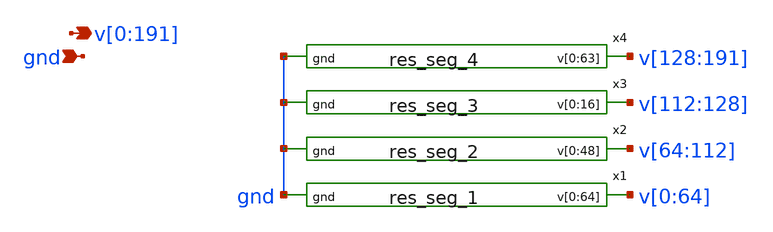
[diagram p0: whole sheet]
** sch_path: xschem/rstring.sch
**.subckt rstring
*+ v[0],v[1],v[2],v[3],v[4],v[5],v[6],v[7],v[8],v[9],v[10],v[11],v[12],v[13],v[14],v[15],v[16],v[17],v[18],v[19],v[20],v[21],v[22],v[23],v[24],v[25],v[26],v[27],v[28],v[29],v[30],v[31],v[32],v[33],v[34],v[35],v[36],v[37],v[38],v[39],v[40],v[41],v[42],v[43],v[44],v[45],v[46],v[47],v[48],v[49],v[50],v[51],v[52],v[53],v[54],v[55],v[56],v[57],v[58],v[59],v[60],v[61],v[62],v[63],v[64],v[65],v[66],v[67],v[68],v[69],v[70],v[71],v[72],v[73],v[74],v[75],v[76],v[77],v[78],v[79],v[80],v[81],v[82],v[83],v[84],v[85],v[86],v[87],v[88],v[89],v[90],v[91],v[92],v[93],v[94],v[95],v[96],v[97],v[98],v[99],v[100],v[101],v[102],v[103],v[104],v[105],v[106],v[107],v[108],v[109],v[110],v[111],v[112],v[113],v[114],v[115],v[116],v[117],v[118],v[119],v[120],v[121],v[122],v[123],v[124],v[125],v[126],v[127],v[128],v[129],v[130],v[131],v[132],v[133],v[134],v[135],v[136],v[137],v[138],v[139],v[140],v[141],v[142],v[143],v[144],v[145],v[146],v[147],v[148],v[149],v[150],v[151],v[152],v[153],v[154],v[155],v[156],v[157],v[158],v[159],v[160],v[161],v[162],v[163],v[164],v[165],v[166],v[167],v[168],v[169],v[170],v[171],v[172],v[173],v[174],v[175],v[176],v[177],v[178],v[179],v[180],v[181],v[182],v[183],v[184],v[185],v[186],v[187],v[188],v[189],v[190],v[191] gnd
*.opin
*+ v[0],v[1],v[2],v[3],v[4],v[5],v[6],v[7],v[8],v[9],v[10],v[11],v[12],v[13],v[14],v[15],v[16],v[17],v[18],v[19],v[20],v[21],v[22],v[23],v[24],v[25],v[26],v[27],v[28],v[29],v[30],v[31],v[32],v[33],v[34],v[35],v[36],v[37],v[38],v[39],v[40],v[41],v[42],v[43],v[44],v[45],v[46],v[47],v[48],v[49],v[50],v[51],v[52],v[53],v[54],v[55],v[56],v[57],v[58],v[59],v[60],v[61],v[62],v[63],v[64],v[65],v[66],v[67],v[68],v[69],v[70],v[71],v[72],v[73],v[74],v[75],v[76],v[77],v[78],v[79],v[80],v[81],v[82],v[83],v[84],v[85],v[86],v[87],v[88],v[89],v[90],v[91],v[92],v[93],v[94],v[95],v[96],v[97],v[98],v[99],v[100],v[101],v[102],v[103],v[104],v[105],v[106],v[107],v[108],v[109],v[110],v[111],v[112],v[113],v[114],v[115],v[116],v[117],v[118],v[119],v[120],v[121],v[122],v[123],v[124],v[125],v[126],v[127],v[128],v[129],v[130],v[131],v[132],v[133],v[134],v[135],v[136],v[137],v[138],v[139],v[140],v[141],v[142],v[143],v[144],v[145],v[146],v[147],v[148],v[149],v[150],v[151],v[152],v[153],v[154],v[155],v[156],v[157],v[158],v[159],v[160],v[161],v[162],v[163],v[164],v[165],v[166],v[167],v[168],v[169],v[170],v[171],v[172],v[173],v[174],v[175],v[176],v[177],v[178],v[179],v[180],v[181],v[182],v[183],v[184],v[185],v[186],v[187],v[188],v[189],v[190],v[191]
*.ipin gnd
x1 v[0] v[1] v[2] v[3] v[4] v[5] v[6] v[7] v[8] v[9] v[10] v[11] v[12] v[13] v[14] v[15] v[16] v[17]
+ v[18] v[19] v[20] v[21] v[22] v[23] v[24] v[25] v[26] v[27] v[28] v[29] v[30] v[31] v[32] v[33] v[34]
+ v[35] v[36] v[37] v[38] v[39] v[40] v[41] v[42] v[43] v[44] v[45] v[46] v[47] v[48] v[49] v[50] v[51]
+ v[52] v[53] v[54] v[55] v[56] v[57] v[58] v[59] v[60] v[61] v[62] v[63] v[64] gnd res_seg_1
x2 v[64] v[65] v[66] v[67] v[68] v[69] v[70] v[71] v[72] v[73] v[74] v[75] v[76] v[77] v[78] v[79]
+ v[80] v[81] v[82] v[83] v[84] v[85] v[86] v[87] v[88] v[89] v[90] v[91] v[92] v[93] v[94] v[95] v[96]
+ v[97] v[98] v[99] v[100] v[101] v[102] v[103] v[104] v[105] v[106] v[107] v[108] v[109] v[110] v[111]
+ v[112] gnd res_seg_2
x3 v[112] v[113] v[114] v[115] v[116] v[117] v[118] v[119] v[120] v[121] v[122] v[123] v[124] v[125]
+ v[126] v[127] v[128] gnd res_seg_3
x4 v[128] v[129] v[130] v[131] v[132] v[133] v[134] v[135] v[136] v[137] v[138] v[139] v[140] v[141]
+ v[142] v[143] v[144] v[145] v[146] v[147] v[148] v[149] v[150] v[151] v[152] v[153] v[154] v[155] v[156]
+ v[157] v[158] v[159] v[160] v[161] v[162] v[163] v[164] v[165] v[166] v[167] v[168] v[169] v[170] v[171]
+ v[172] v[173] v[174] v[175] v[176] v[177] v[178] v[179] v[180] v[181] v[182] v[183] v[184] v[185] v[186]
+ v[187] v[188] v[189] v[190] v[191] gnd res_seg_4
**.ends

* expanding   symbol:  res_seg_1.sym # of pins=2
** sym_path: xschem/res_seg_1.sym
** sch_path: xschem/res_seg_1.sch
.subckt res_seg_1 v[0] v[1] v[2] v[3] v[4] v[5] v[6] v[7] v[8] v[9] v[10] v[11] v[12] v[13] v[14]
+ v[15] v[16] v[17] v[18] v[19] v[20] v[21] v[22] v[23] v[24] v[25] v[26] v[27] v[28] v[29] v[30] v[31]
+ v[32] v[33] v[34] v[35] v[36] v[37] v[38] v[39] v[40] v[41] v[42] v[43] v[44] v[45] v[46] v[47] v[48]
+ v[49] v[50] v[51] v[52] v[53] v[54] v[55] v[56] v[57] v[58] v[59] v[60] v[61] v[62] v[63] v[64] gnd
*.opin
*+ v[0],v[1],v[2],v[3],v[4],v[5],v[6],v[7],v[8],v[9],v[10],v[11],v[12],v[13],v[14],v[15],v[16],v[17],v[18],v[19],v[20],v[21],v[22],v[23],v[24],v[25],v[26],v[27],v[28],v[29],v[30],v[31],v[32],v[33],v[34],v[35],v[36],v[37],v[38],v[39],v[40],v[41],v[42],v[43],v[44],v[45],v[46],v[47],v[48],v[49],v[50],v[51],v[52],v[53],v[54],v[55],v[56],v[57],v[58],v[59],v[60],v[61],v[62],v[63],v[64]
*.ipin gnd
XR1 v[1] v[0] gnd sky130_fd_pr__res_xhigh_po_0p35 L=0.8375 mult=1 m=1
XR2 v[2] v[1] gnd sky130_fd_pr__res_xhigh_po_0p35 L=0.7349 mult=1 m=1
XR3 v[3] v[2] gnd sky130_fd_pr__res_xhigh_po_0p35 L=0.6495 mult=1 m=1
XR4 v[4] v[3] gnd sky130_fd_pr__res_xhigh_po_0p35 L=0.5897 mult=1 m=1
XR8 v[7] v[8] gnd sky130_fd_pr__res_xhigh_po_0p69 L=0.8761 mult=1 m=1
XR9 v[8] v[9] gnd sky130_fd_pr__res_xhigh_po_0p69 L=0.8255 mult=1 m=1
XR10 v[9] v[10] gnd sky130_fd_pr__res_xhigh_po_0p69 L=0.775 mult=1 m=1
XR11 v[10] v[11] gnd sky130_fd_pr__res_xhigh_po_0p69 L=0.7413 mult=1 m=1
XR12 v[11] v[12] gnd sky130_fd_pr__res_xhigh_po_0p69 L=0.7076 mult=1 m=1
XR13 v[12] v[13] gnd sky130_fd_pr__res_xhigh_po_0p69 L=0.6739 mult=1 m=1
XR14 v[13] v[14] gnd sky130_fd_pr__res_xhigh_po_0p69 L=0.657 mult=1 m=1
XR15 v[14] v[15] gnd sky130_fd_pr__res_xhigh_po_0p69 L=0.6234 mult=1 m=1
XR16 v[15] v[16] gnd sky130_fd_pr__res_xhigh_po_0p69 L=0.6065 mult=1 m=1
XR17 v[16] v[17] gnd sky130_fd_pr__res_xhigh_po_0p69 L=0.5728 mult=1 m=1
XR19 v[18] v[19] gnd sky130_fd_pr__res_xhigh_po_0p69 L=0.5391 mult=1 m=1
XR27 v[26] v[27] gnd sky130_fd_pr__res_xhigh_po_1p41 L=0.8951 mult=1 m=1
XR29 v[28] v[29] gnd sky130_fd_pr__res_xhigh_po_1p41 L=0.8607 mult=1 m=1
XR31 v[30] v[31] gnd sky130_fd_pr__res_xhigh_po_1p41 L=0.8263 mult=1 m=1
XR33 v[32] v[33] gnd sky130_fd_pr__res_xhigh_po_1p41 L=0.7918 mult=1 m=1
XR36 v[35] v[36] gnd sky130_fd_pr__res_xhigh_po_1p41 L=0.7574 mult=1 m=1
XR37 v[36] v[37] gnd sky130_fd_pr__res_xhigh_po_1p41 L=0.723 mult=1 m=1
XR40 v[39] v[40] gnd sky130_fd_pr__res_xhigh_po_1p41 L=0.6885 mult=1 m=1
XR41 v[40] v[41] gnd sky130_fd_pr__res_xhigh_po_1p41 L=0.723 mult=1 m=1
XR42 v[41] v[42] gnd sky130_fd_pr__res_xhigh_po_1p41 L=0.6885 mult=1 m=1
XR43 v[42] v[43] gnd sky130_fd_pr__res_xhigh_po_1p41 L=0.6541 mult=1 m=1
XR45 v[44] v[45] gnd sky130_fd_pr__res_xhigh_po_1p41 L=0.6541 mult=1 m=1
XR48 v[47] v[48] gnd sky130_fd_pr__res_xhigh_po_1p41 L=0.6197 mult=1 m=1
XR49 v[48] v[49] gnd sky130_fd_pr__res_xhigh_po_1p41 L=0.6541 mult=1 m=1
XR51 v[50] v[51] gnd sky130_fd_pr__res_xhigh_po_1p41 L=0.5853 mult=1 m=1
XR52 v[51] v[52] gnd sky130_fd_pr__res_xhigh_po_1p41 L=0.6197 mult=1 m=1
XR53 v[52] v[53] gnd sky130_fd_pr__res_xhigh_po_1p41 L=0.5853 mult=1 m=1
XR58 v[57] v[58] gnd sky130_fd_pr__res_xhigh_po_1p41 L=0.5508 mult=1 m=1
XR64 v[63] v[64] gnd sky130_fd_pr__res_xhigh_po_1p41 L=0.5164 mult=1 m=1
XR5 v[5] v[4] gnd sky130_fd_pr__res_xhigh_po_0p35 L=0.5469 mult=1 m=1
XR6 v[6] v[5] gnd sky130_fd_pr__res_xhigh_po_0p35 L=0.5042 mult=1 m=1
XR21 v[20] v[21] gnd sky130_fd_pr__res_xhigh_po_0p69 L=0.5054 mult=1 m=1
XR54 v[53] v[54] gnd sky130_fd_pr__res_xhigh_po_1p41 L=0.5853 mult=1 m=1
XR7 v[6] v[7] gnd sky130_fd_pr__res_xhigh_po_0p69 L=0.9266 mult=1 m=1
XR18 v[17] v[18] gnd sky130_fd_pr__res_xhigh_po_0p69 L=0.5728 mult=1 m=1
XR20 v[19] v[20] gnd sky130_fd_pr__res_xhigh_po_0p69 L=0.5391 mult=1 m=1
XR22 v[21] v[22] gnd sky130_fd_pr__res_xhigh_po_0p69 L=0.5054 mult=1 m=1
XR23 v[22] v[23] gnd sky130_fd_pr__res_xhigh_po_1p41 L=0.9984 mult=1 m=1
XR24 v[23] v[24] gnd sky130_fd_pr__res_xhigh_po_1p41 L=0.9984 mult=1 m=1
XR25 v[24] v[25] gnd sky130_fd_pr__res_xhigh_po_1p41 L=0.9295 mult=1 m=1
XR26 v[25] v[26] gnd sky130_fd_pr__res_xhigh_po_1p41 L=0.9295 mult=1 m=1
XR28 v[27] v[28] gnd sky130_fd_pr__res_xhigh_po_1p41 L=0.8951 mult=1 m=1
XR30 v[29] v[30] gnd sky130_fd_pr__res_xhigh_po_1p41 L=0.8607 mult=1 m=1
XR32 v[31] v[32] gnd sky130_fd_pr__res_xhigh_po_1p41 L=0.8263 mult=1 m=1
XR34 v[33] v[34] gnd sky130_fd_pr__res_xhigh_po_1p41 L=0.7918 mult=1 m=1
XR35 v[34] v[35] gnd sky130_fd_pr__res_xhigh_po_1p41 L=0.7918 mult=1 m=1
XR38 v[37] v[38] gnd sky130_fd_pr__res_xhigh_po_1p41 L=0.7574 mult=1 m=1
XR39 v[38] v[39] gnd sky130_fd_pr__res_xhigh_po_1p41 L=0.723 mult=1 m=1
XR44 v[43] v[44] gnd sky130_fd_pr__res_xhigh_po_1p41 L=0.6885 mult=1 m=1
XR46 v[45] v[46] gnd sky130_fd_pr__res_xhigh_po_1p41 L=0.6541 mult=1 m=1
XR47 v[46] v[47] gnd sky130_fd_pr__res_xhigh_po_1p41 L=0.6541 mult=1 m=1
XR50 v[49] v[50] gnd sky130_fd_pr__res_xhigh_po_1p41 L=0.6197 mult=1 m=1
XR55 v[54] v[55] gnd sky130_fd_pr__res_xhigh_po_1p41 L=0.5853 mult=1 m=1
XR56 v[55] v[56] gnd sky130_fd_pr__res_xhigh_po_1p41 L=0.5853 mult=1 m=1
XR57 v[56] v[57] gnd sky130_fd_pr__res_xhigh_po_1p41 L=0.5853 mult=1 m=1
XR59 v[58] v[59] gnd sky130_fd_pr__res_xhigh_po_1p41 L=0.5508 mult=1 m=1
XR60 v[59] v[60] gnd sky130_fd_pr__res_xhigh_po_1p41 L=0.5508 mult=1 m=1
XR61 v[60] v[61] gnd sky130_fd_pr__res_xhigh_po_1p41 L=0.5508 mult=1 m=1
XR62 v[61] v[62] gnd sky130_fd_pr__res_xhigh_po_1p41 L=0.5508 mult=1 m=1
XR63 v[62] v[63] gnd sky130_fd_pr__res_xhigh_po_1p41 L=0.5508 mult=1 m=1
.ends


* expanding   symbol:  res_seg_2.sym # of pins=2
** sym_path: xschem/res_seg_2.sym
** sch_path: xschem/res_seg_2.sch
.subckt res_seg_2 v[0] v[1] v[2] v[3] v[4] v[5] v[6] v[7] v[8] v[9] v[10] v[11] v[12] v[13] v[14]
+ v[15] v[16] v[17] v[18] v[19] v[20] v[21] v[22] v[23] v[24] v[25] v[26] v[27] v[28] v[29] v[30] v[31]
+ v[32] v[33] v[34] v[35] v[36] v[37] v[38] v[39] v[40] v[41] v[42] v[43] v[44] v[45] v[46] v[47] v[48] gnd
*.opin
*+ v[0],v[1],v[2],v[3],v[4],v[5],v[6],v[7],v[8],v[9],v[10],v[11],v[12],v[13],v[14],v[15],v[16],v[17],v[18],v[19],v[20],v[21],v[22],v[23],v[24],v[25],v[26],v[27],v[28],v[29],v[30],v[31],v[32],v[33],v[34],v[35],v[36],v[37],v[38],v[39],v[40],v[41],v[42],v[43],v[44],v[45],v[46],v[47],v[48]
*.ipin gnd
XR1 v[1] v[0] gnd sky130_fd_pr__res_xhigh_po_0p35 L=1.9570 mult=1 m=1
XR2 v[2] v[1] gnd sky130_fd_pr__res_xhigh_po_0p35 L=1.7348 mult=1 m=1
XR3 v[3] v[2] gnd sky130_fd_pr__res_xhigh_po_0p35 L=1.5639 mult=1 m=1
XR4 v[4] v[3] gnd sky130_fd_pr__res_xhigh_po_0p35 L=1.4442 mult=1 m=1
XR5 v[5] v[4] gnd sky130_fd_pr__res_xhigh_po_0p35 L=1.3417 mult=1 m=1
XR6 v[6] v[5] gnd sky130_fd_pr__res_xhigh_po_0p35 L=1.2648 mult=1 m=1
XR7 v[7] v[6] gnd sky130_fd_pr__res_xhigh_po_0p35 L=1.1964 mult=1 m=1
XR8 v[8] v[7] gnd sky130_fd_pr__res_xhigh_po_0p35 L=1.1366 mult=1 m=1
XR9 v[9] v[8] gnd sky130_fd_pr__res_xhigh_po_0p35 L=1.0853 mult=1 m=1
XR10 v[10] v[9] gnd sky130_fd_pr__res_xhigh_po_0p35 L=1.0511 mult=1 m=1
XR11 v[11] v[10] gnd sky130_fd_pr__res_xhigh_po_0p35 L=1.0169 mult=1 m=1
XR12 v[12] v[11] gnd sky130_fd_pr__res_xhigh_po_0p35 L=0.9828 mult=1 m=1
XR13 v[13] v[12] gnd sky130_fd_pr__res_xhigh_po_0p35 L=0.9571 mult=1 m=1
XR14 v[14] v[13] gnd sky130_fd_pr__res_xhigh_po_0p35 L=0.94 mult=1 m=1
XR15 v[15] v[14] gnd sky130_fd_pr__res_xhigh_po_0p35 L=0.9144 mult=1 m=1
XR16 v[16] v[15] gnd sky130_fd_pr__res_xhigh_po_0p35 L=0.8888 mult=1 m=1
XR17 v[17] v[16] gnd sky130_fd_pr__res_xhigh_po_0p35 L=0.8802 mult=1 m=1
XR18 v[18] v[17] gnd sky130_fd_pr__res_xhigh_po_0p35 L=0.8717 mult=1 m=1
XR19 v[19] v[18] gnd sky130_fd_pr__res_xhigh_po_0p35 L=0.8546 mult=1 m=1
XR20 v[20] v[19] gnd sky130_fd_pr__res_xhigh_po_0p35 L=0.8375 mult=1 m=1
XR22 v[22] v[21] gnd sky130_fd_pr__res_xhigh_po_0p35 L=0.8289 mult=1 m=1
XR23 v[23] v[22] gnd sky130_fd_pr__res_xhigh_po_0p35 L=0.8204 mult=1 m=1
XR24 v[24] v[23] gnd sky130_fd_pr__res_xhigh_po_0p35 L=0.8118 mult=1 m=1
XR33 v[33] v[32] gnd sky130_fd_pr__res_xhigh_po_0p35 L=0.8204 mult=1 m=1
XR35 v[35] v[34] gnd sky130_fd_pr__res_xhigh_po_0p35 L=0.8289 mult=1 m=1
XR36 v[36] v[35] gnd sky130_fd_pr__res_xhigh_po_0p35 L=0.8375 mult=1 m=1
XR38 v[38] v[37] gnd sky130_fd_pr__res_xhigh_po_0p35 L=0.8631 mult=1 m=1
XR40 v[40] v[39] gnd sky130_fd_pr__res_xhigh_po_0p35 L=0.8888 mult=1 m=1
XR41 v[41] v[40] gnd sky130_fd_pr__res_xhigh_po_0p35 L=0.8973 mult=1 m=1
XR42 v[42] v[41] gnd sky130_fd_pr__res_xhigh_po_0p35 L=0.9144 mult=1 m=1
XR43 v[43] v[42] gnd sky130_fd_pr__res_xhigh_po_0p35 L=0.94 mult=1 m=1
XR44 v[44] v[43] gnd sky130_fd_pr__res_xhigh_po_0p35 L=0.9571 mult=1 m=1
XR45 v[45] v[44] gnd sky130_fd_pr__res_xhigh_po_0p35 L=0.9828 mult=1 m=1
XR46 v[46] v[45] gnd sky130_fd_pr__res_xhigh_po_0p35 L=1.0084 mult=1 m=1
XR47 v[47] v[46] gnd sky130_fd_pr__res_xhigh_po_0p35 L=1.0426 mult=1 m=1
XR48 v[48] v[47] gnd sky130_fd_pr__res_xhigh_po_0p35 L=1.0853 mult=1 m=1
XR37 v[37] v[36] gnd sky130_fd_pr__res_xhigh_po_0p35 L=0.846 mult=1 m=1
XR21 v[21] v[20] gnd sky130_fd_pr__res_xhigh_po_0p35 L=0.8375 mult=1 m=1
XR25 v[25] v[24] gnd sky130_fd_pr__res_xhigh_po_0p35 L=0.8118 mult=1 m=1
XR26 v[26] v[25] gnd sky130_fd_pr__res_xhigh_po_0p35 L=0.8118 mult=1 m=1
XR27 v[27] v[26] gnd sky130_fd_pr__res_xhigh_po_0p35 L=0.8033 mult=1 m=1
XR28 v[28] v[27] gnd sky130_fd_pr__res_xhigh_po_0p35 L=0.8118 mult=1 m=1
XR29 v[29] v[28] gnd sky130_fd_pr__res_xhigh_po_0p35 L=0.8033 mult=1 m=1
XR30 v[30] v[29] gnd sky130_fd_pr__res_xhigh_po_0p35 L=0.8033 mult=1 m=1
XR31 v[31] v[30] gnd sky130_fd_pr__res_xhigh_po_0p35 L=0.8118 mult=1 m=1
XR32 v[32] v[31] gnd sky130_fd_pr__res_xhigh_po_0p35 L=0.8118 mult=1 m=1
XR34 v[34] v[33] gnd sky130_fd_pr__res_xhigh_po_0p35 L=0.8204 mult=1 m=1
XR39 v[39] v[38] gnd sky130_fd_pr__res_xhigh_po_0p35 L=0.8631 mult=1 m=1
.ends


* expanding   symbol:  res_seg_3.sym # of pins=2
** sym_path: xschem/res_seg_3.sym
** sch_path: xschem/res_seg_3.sch
.subckt res_seg_3 v[0] v[1] v[2] v[3] v[4] v[5] v[6] v[7] v[8] v[9] v[10] v[11] v[12] v[13] v[14]
+ v[15] v[16] gnd
*.opin v[0],v[1],v[2],v[3],v[4],v[5],v[6],v[7],v[8],v[9],v[10],v[11],v[12],v[13],v[14],v[15],v[16]
*.ipin gnd
XR1 v[0] v[1] gnd sky130_fd_pr__res_xhigh_po_0p35 L=0.5555 mult=1 m=1
XR2 v[1] v[2] gnd sky130_fd_pr__res_xhigh_po_0p35 L=0.5726 mult=1 m=1
XR3 v[2] v[3] gnd sky130_fd_pr__res_xhigh_po_0p35 L=0.5811 mult=1 m=1
XR4 v[3] v[4] gnd sky130_fd_pr__res_xhigh_po_0p35 L=0.5897 mult=1 m=1
XR5 v[4] v[5] gnd sky130_fd_pr__res_xhigh_po_0p35 L=0.6153 mult=1 m=1
XR6 v[5] v[6] gnd sky130_fd_pr__res_xhigh_po_0p35 L=0.6238 mult=1 m=1
XR7 v[6] v[7] gnd sky130_fd_pr__res_xhigh_po_0p35 L=0.6409 mult=1 m=1
XR8 v[7] v[8] gnd sky130_fd_pr__res_xhigh_po_0p35 L=0.6666 mult=1 m=1
XR9 v[8] v[9] gnd sky130_fd_pr__res_xhigh_po_0p35 L=0.6837 mult=1 m=1
XR10 v[9] v[10] gnd sky130_fd_pr__res_xhigh_po_0p35 L=0.7093 mult=1 m=1
XR11 v[10] v[11] gnd sky130_fd_pr__res_xhigh_po_0p35 L=0.7264 mult=1 m=1
XR12 v[11] v[12] gnd sky130_fd_pr__res_xhigh_po_0p35 L=0.7691 mult=1 m=1
XR13 v[12] v[13] gnd sky130_fd_pr__res_xhigh_po_0p35 L=0.7948 mult=1 m=1
XR14 v[13] v[14] gnd sky130_fd_pr__res_xhigh_po_0p35 L=0.8375 mult=1 m=1
XR15 v[14] v[15] gnd sky130_fd_pr__res_xhigh_po_0p35 L=0.8802 mult=1 m=1
XR16 v[15] v[16] gnd sky130_fd_pr__res_xhigh_po_0p35 L=0.9315 mult=1 m=1
.ends


* expanding   symbol:  res_seg_4.sym # of pins=2
** sym_path: xschem/res_seg_4.sym
** sch_path: xschem/res_seg_4.sch
.subckt res_seg_4 v[0] v[1] v[2] v[3] v[4] v[5] v[6] v[7] v[8] v[9] v[10] v[11] v[12] v[13] v[14]
+ v[15] v[16] v[17] v[18] v[19] v[20] v[21] v[22] v[23] v[24] v[25] v[26] v[27] v[28] v[29] v[30] v[31]
+ v[32] v[33] v[34] v[35] v[36] v[37] v[38] v[39] v[40] v[41] v[42] v[43] v[44] v[45] v[46] v[47] v[48]
+ v[49] v[50] v[51] v[52] v[53] v[54] v[55] v[56] v[57] v[58] v[59] v[60] v[61] v[62] v[63] gnd
*.opin
*+ v[0],v[1],v[2],v[3],v[4],v[5],v[6],v[7],v[8],v[9],v[10],v[11],v[12],v[13],v[14],v[15],v[16],v[17],v[18],v[19],v[20],v[21],v[22],v[23],v[24],v[25],v[26],v[27],v[28],v[29],v[30],v[31],v[32],v[33],v[34],v[35],v[36],v[37],v[38],v[39],v[40],v[41],v[42],v[43],v[44],v[45],v[46],v[47],v[48],v[49],v[50],v[51],v[52],v[53],v[54],v[55],v[56],v[57],v[58],v[59],v[60],v[61],v[62],v[63]
*.ipin gnd
XR7 v[6] v[7] gnd sky130_fd_pr__res_xhigh_po_1p41 L=0.5164 mult=1 m=1
XR10 v[9] v[10] gnd sky130_fd_pr__res_xhigh_po_1p41 L=0.5508 mult=1 m=1
XR17 v[16] v[17] gnd sky130_fd_pr__res_xhigh_po_1p41 L=0.5853 mult=1 m=1
XR28 v[27] v[28] gnd sky130_fd_pr__res_xhigh_po_1p41 L=0.6541 mult=1 m=1
XR31 v[30] v[31] gnd sky130_fd_pr__res_xhigh_po_1p41 L=0.6885 mult=1 m=1
XR36 v[35] v[36] gnd sky130_fd_pr__res_xhigh_po_1p41 L=0.7574 mult=1 m=1
XR37 v[36] v[37] gnd sky130_fd_pr__res_xhigh_po_1p41 L=0.723 mult=1 m=1
XR40 v[39] v[40] gnd sky130_fd_pr__res_xhigh_po_1p41 L=0.7918 mult=1 m=1
XR43 v[42] v[43] gnd sky130_fd_pr__res_xhigh_po_1p41 L=0.8263 mult=1 m=1
XR44 v[43] v[44] gnd sky130_fd_pr__res_xhigh_po_1p41 L=0.8607 mult=1 m=1
XR46 v[45] v[46] gnd sky130_fd_pr__res_xhigh_po_1p41 L=0.8951 mult=1 m=1
XR51 v[50] v[51] gnd sky130_fd_pr__res_xhigh_po_0p69 L=0.5054 mult=1 m=1
XR53 v[52] v[53] gnd sky130_fd_pr__res_xhigh_po_0p69 L=0.5391 mult=1 m=1
XR55 v[54] v[55] gnd sky130_fd_pr__res_xhigh_po_0p69 L=0.5728 mult=1 m=1
XR56 v[55] v[56] gnd sky130_fd_pr__res_xhigh_po_0p69 L=0.5897 mult=1 m=1
XR57 v[56] v[57] gnd sky130_fd_pr__res_xhigh_po_0p69 L=0.6234 mult=1 m=1
XR58 v[57] v[58] gnd sky130_fd_pr__res_xhigh_po_0p69 L=0.6402 mult=1 m=1
XR59 v[58] v[59] gnd sky130_fd_pr__res_xhigh_po_0p69 L=0.6907 mult=1 m=1
XR60 v[59] v[60] gnd sky130_fd_pr__res_xhigh_po_0p69 L=0.7244 mult=1 m=1
XR61 v[60] v[61] gnd sky130_fd_pr__res_xhigh_po_0p69 L=0.7581 mult=1 m=1
XR8 v[7] v[8] gnd sky130_fd_pr__res_xhigh_po_1p41 L=0.5164 mult=1 m=1
XR11 v[10] v[11] gnd sky130_fd_pr__res_xhigh_po_1p41 L=0.5164 mult=1 m=1
XR12 v[11] v[12] gnd sky130_fd_pr__res_xhigh_po_1p41 L=0.5508 mult=1 m=1
XR13 v[12] v[13] gnd sky130_fd_pr__res_xhigh_po_1p41 L=0.5164 mult=1 m=1
XR23 v[22] v[23] gnd sky130_fd_pr__res_xhigh_po_1p41 L=0.6197 mult=1 m=1
XR34 v[33] v[34] gnd sky130_fd_pr__res_xhigh_po_1p41 L=0.723 mult=1 m=1
XR41 v[40] v[41] gnd sky130_fd_pr__res_xhigh_po_1p41 L=0.7918 mult=1 m=1
XR1 v[0] v[1] gnd sky130_fd_pr__res_xhigh_po_2p85 L=0.9742 mult=1 m=1
XR2 v[1] v[2] gnd sky130_fd_pr__res_xhigh_po_2p85 L=0.9742 mult=1 m=1
XR4 v[3] v[4] gnd sky130_fd_pr__res_xhigh_po_2p85 L=0.9742 mult=1 m=1
XR6 v[5] v[6] gnd sky130_fd_pr__res_xhigh_po_2p85 L=0.9742 mult=1 m=1
XR3 v[2] v[3] gnd sky130_fd_pr__res_xhigh_po_2p85 L=1.0438 mult=1 m=1
XR5 v[4] v[5] gnd sky130_fd_pr__res_xhigh_po_2p85 L=1.0438 mult=1 m=1
XR9 v[8] v[9] gnd sky130_fd_pr__res_xhigh_po_1p41 L=0.5164 mult=1 m=1
XR14 v[13] v[14] gnd sky130_fd_pr__res_xhigh_po_1p41 L=0.5508 mult=1 m=1
XR15 v[14] v[15] gnd sky130_fd_pr__res_xhigh_po_1p41 L=0.5508 mult=1 m=1
XR16 v[15] v[16] gnd sky130_fd_pr__res_xhigh_po_1p41 L=0.5508 mult=1 m=1
XR18 v[17] v[18] gnd sky130_fd_pr__res_xhigh_po_1p41 L=0.5508 mult=1 m=1
XR19 v[18] v[19] gnd sky130_fd_pr__res_xhigh_po_1p41 L=0.5853 mult=1 m=1
XR20 v[19] v[20] gnd sky130_fd_pr__res_xhigh_po_1p41 L=0.5853 mult=1 m=1
XR21 v[20] v[21] gnd sky130_fd_pr__res_xhigh_po_1p41 L=0.5853 mult=1 m=1
XR22 v[21] v[22] gnd sky130_fd_pr__res_xhigh_po_1p41 L=0.5853 mult=1 m=1
XR24 v[23] v[24] gnd sky130_fd_pr__res_xhigh_po_1p41 L=0.6197 mult=1 m=1
XR25 v[24] v[25] gnd sky130_fd_pr__res_xhigh_po_1p41 L=0.6197 mult=1 m=1
XR26 v[25] v[26] gnd sky130_fd_pr__res_xhigh_po_1p41 L=0.6197 mult=1 m=1
XR27 v[26] v[27] gnd sky130_fd_pr__res_xhigh_po_1p41 L=0.6197 mult=1 m=1
XR29 v[28] v[29] gnd sky130_fd_pr__res_xhigh_po_1p41 L=0.6541 mult=1 m=1
XR30 v[29] v[30] gnd sky130_fd_pr__res_xhigh_po_1p41 L=0.6541 mult=1 m=1
XR32 v[31] v[32] gnd sky130_fd_pr__res_xhigh_po_1p41 L=0.6541 mult=1 m=1
XR33 v[32] v[33] gnd sky130_fd_pr__res_xhigh_po_1p41 L=0.6885 mult=1 m=1
XR35 v[34] v[35] gnd sky130_fd_pr__res_xhigh_po_1p41 L=0.6885 mult=1 m=1
XR38 v[37] v[38] gnd sky130_fd_pr__res_xhigh_po_1p41 L=0.7574 mult=1 m=1
XR39 v[38] v[39] gnd sky130_fd_pr__res_xhigh_po_1p41 L=0.7574 mult=1 m=1
XR42 v[41] v[42] gnd sky130_fd_pr__res_xhigh_po_1p41 L=0.7918 mult=1 m=1
XR45 v[44] v[45] gnd sky130_fd_pr__res_xhigh_po_1p41 L=0.8607 mult=1 m=1
XR47 v[46] v[47] gnd sky130_fd_pr__res_xhigh_po_1p41 L=0.8951 mult=1 m=1
XR48 v[47] v[48] gnd sky130_fd_pr__res_xhigh_po_1p41 L=0.9295 mult=1 m=1
XR49 v[48] v[49] gnd sky130_fd_pr__res_xhigh_po_1p41 L=0.964 mult=1 m=1
XR50 v[49] v[50] gnd sky130_fd_pr__res_xhigh_po_1p41 L=0.964 mult=1 m=1
XR52 v[51] v[52] gnd sky130_fd_pr__res_xhigh_po_0p69 L=0.5054 mult=1 m=1
XR54 v[53] v[54] gnd sky130_fd_pr__res_xhigh_po_0p69 L=0.5391 mult=1 m=1
XR62 v[61] v[62] gnd sky130_fd_pr__res_xhigh_po_0p69 L=0.8424 mult=1 m=1
XR63 v[62] v[63] gnd sky130_fd_pr__res_xhigh_po_0p69 L=0.8929 mult=1 m=1
.ends

.end
